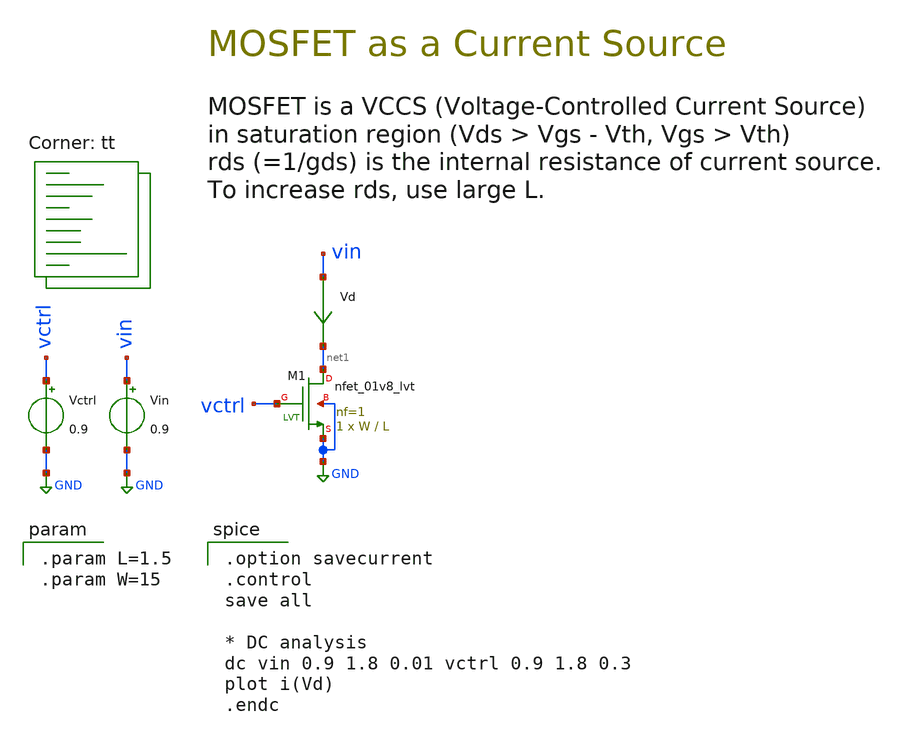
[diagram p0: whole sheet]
** sch_path: 00-f_current-source.sch
**.subckt 00-f_current-source
XM1 net1 vctrl GND GND sky130_fd_pr__nfet_01v8_lvt L=L W=W nf=1 ad='int((1 + 1)/2) * W / 1 * 0.29' as='int((1 + 2)/2) * W / 1 * 0.29'
+ pd='2*int((1 + 1)/2) * (W / 1 + 0.29)' ps='2*int((1 + 2)/2) * (W / 1 + 0.29)' nrd='0.29 / W ' nrs='0.29 / W '
+ sa=0 sb=0 sd=0 mult=1 m=1
Vctrl vctrl GND 0.9
Vin vin GND 0.9
Vd vin net1 0
.save i(vd)
**** begin user architecture code
.lib $::SKYWATER_MODELS/sky130.lib.spice tt

.param L=1.5
.param W=15


.option savecurrent
.control
save all

* DC analysis
dc vin 0.9 1.8 0.01 vctrl 0.9 1.8 0.3
plot i(Vd)
.endc

**** end user architecture code
**.ends
.GLOBAL GND
.end
